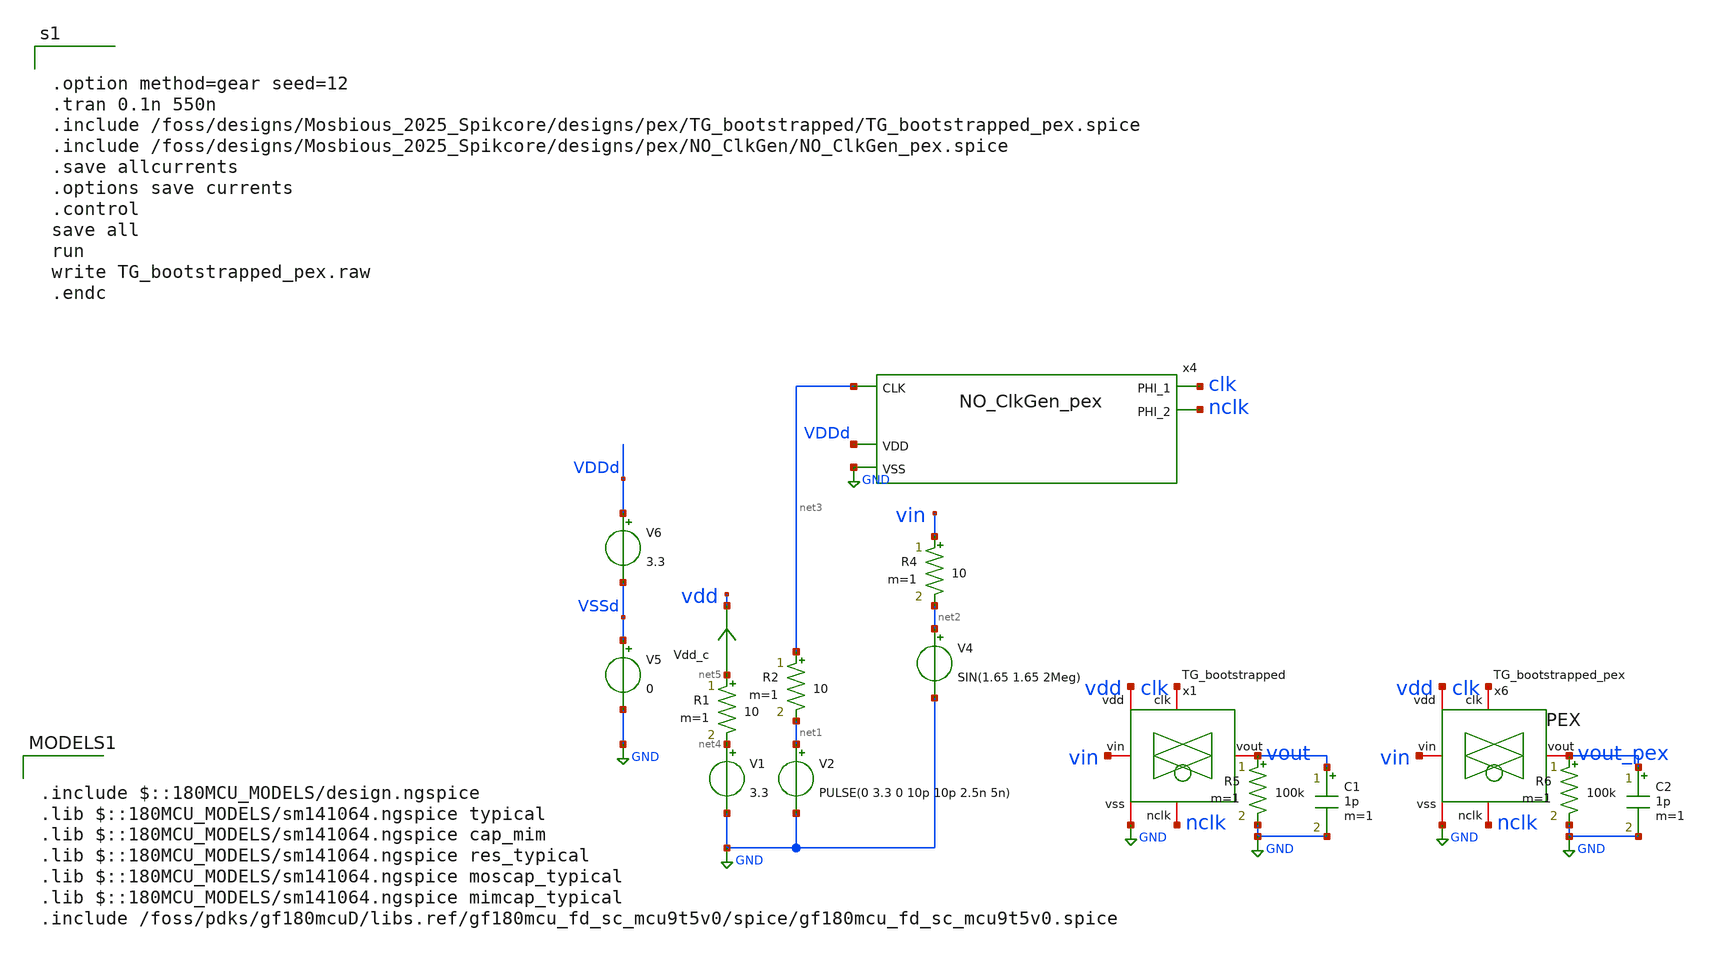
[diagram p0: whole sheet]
** sch_path: designs/pex/TG_bootstrapped/TG_bootstrapped_pex.sch
**.subckt TG_bootstrapped_pex
x1 vdd GND clk nclk vin vout TG_bootstrapped
V1 net4 GND 3.3
Vdd_c net5 vdd 0
.save i(vdd_c)
R1 net5 net4 10 m=1
V2 net1 GND PULSE(0 3.3 0 10p 10p 2.5n 5n)
R2 net3 net1 10 m=1
V4 net2 GND SIN(1.65 1.65 2Meg)
R4 vin net2 10 m=1
R5 vout GND 100k m=1
V5 VSSd GND 0
V6 VDDd VSSd 3.3
C1 vout GND 1p m=1
R6 vout_pex GND 100k m=1
C2 vout_pex GND 1p m=1
x6 vdd GND clk nclk vin vout_pex TG_bootstrapped_pex
x4 nclk net3 clk VDDd GND NO_ClkGen_pex
**** begin user architecture code


.option method=gear seed=12
.tran 0.1n 550n
.include /foss/designs/Mosbious_2025_Spikcore/designs/pex/TG_bootstrapped/TG_bootstrapped_pex.spice
.include /foss/designs/Mosbious_2025_Spikcore/designs/pex/NO_ClkGen/NO_ClkGen_pex.spice
.save allcurrents
.options save currents
.control
save all
run
write TG_bootstrapped_pex.raw
.endc



.include $::180MCU_MODELS/design.ngspice
.lib $::180MCU_MODELS/sm141064.ngspice typical
.lib $::180MCU_MODELS/sm141064.ngspice cap_mim
.lib $::180MCU_MODELS/sm141064.ngspice res_typical
.lib $::180MCU_MODELS/sm141064.ngspice moscap_typical
.lib $::180MCU_MODELS/sm141064.ngspice mimcap_typical
.include /foss/pdks/gf180mcuD/libs.ref/gf180mcu_fd_sc_mcu9t5v0/spice/gf180mcu_fd_sc_mcu9t5v0.spice

**** end user architecture code
**.ends
.GLOBAL GND
.end
